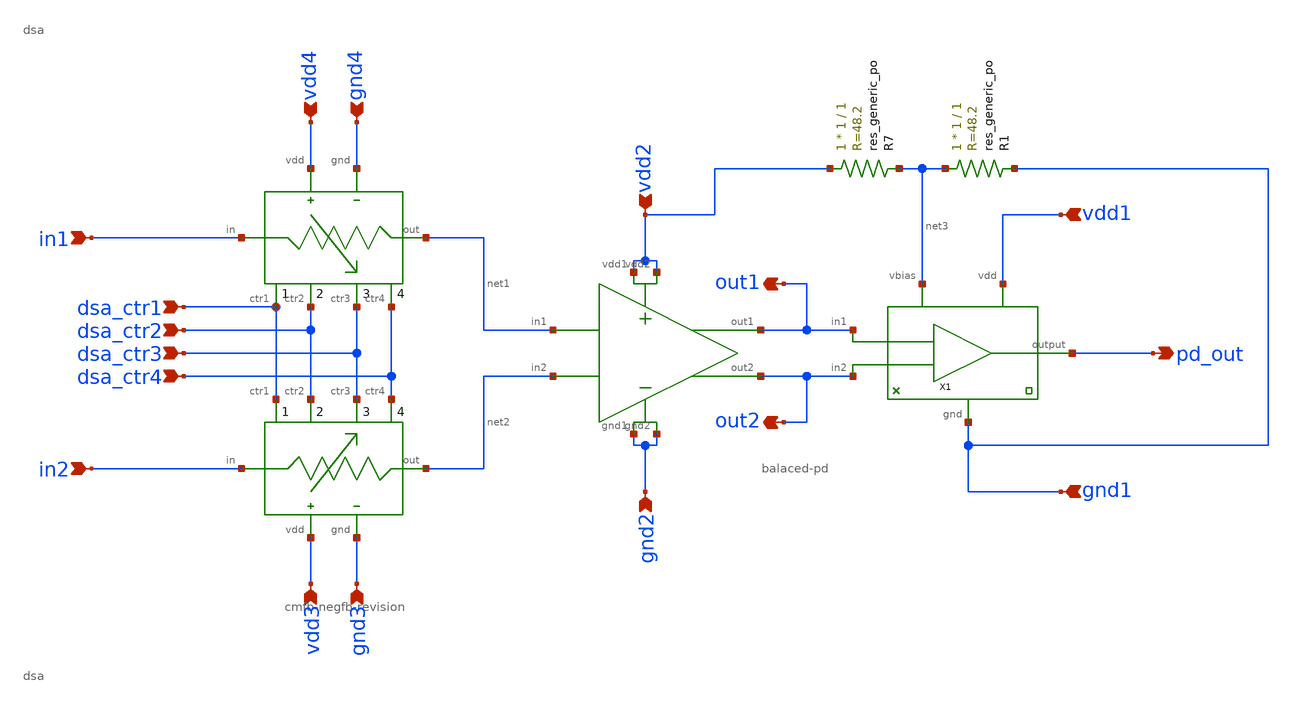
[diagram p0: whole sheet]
** sch_path: xschem/user_analog_project_wrapper.sch
**.subckt user_analog_project_wrapper in1 in2 vdd1 gnd1 dsa_ctr1 dsa_ctr2 dsa_ctr3 dsa_ctr4 pd_out
*+ out1 out2 gnd2 gnd3 gnd4 vdd2 vdd3 vdd4
*.ipin in1
*.ipin in2
*.ipin vdd1
*.ipin gnd1
*.ipin dsa_ctr1
*.ipin dsa_ctr2
*.ipin dsa_ctr3
*.ipin dsa_ctr4
*.opin pd_out
*.opin out1
*.opin out2
*.ipin gnd2
*.ipin gnd3
*.ipin gnd4
*.ipin vdd2
*.ipin vdd3
*.ipin vdd4
XDSA1 dsa_ctr1 dsa_ctr2 dsa_ctr3 dsa_ctr4 in2 vdd3 gnd3 net2 dsa
XDSA2 dsa_ctr1 dsa_ctr2 dsa_ctr3 dsa_ctr4 in1 vdd4 gnd4 net1 dsa
XLNA1 vdd2 vdd2 net1 net2 out1 out2 gnd2 gnd2 cmfb-negfb-revision
X1 out1 out2 net3 vdd1 pd_out gnd1 balaced-pd
XR7 vdd2 net3 sky130_fd_pr__res_generic_po W=1 L=1 m=1
XR1 net3 gnd1 sky130_fd_pr__res_generic_po W=1 L=1 m=1
**** begin user architecture code
 ** manual skywater pdks install (with patches applied)
* .lib $::SKYWATER_MODELS/models/sky130.lib.spice tt

** opencircuitdesign pdks install
.lib $::SKYWATER_MODELS/sky130.lib.spice tt

.param mc_mm_switch=0
.param mc_pr_switch=0

**** end user architecture code
**.ends

* expanding   symbol:  /Volumes/WORK_DRIVE/caravel_automatic_gain_control/xschem/attenuator/dsa.sym
*+ # of pins=8
** sym_path: xschem/attenuator/dsa.sym
** sch_path: xschem/attenuator/dsa.sch
.subckt dsa ctr1 ctr2 ctr3 ctr4 in vdd gnd out
*.ipin in
*.ipin gnd
*.ipin vdd
*.ipin ctr1
*.ipin ctr2
*.ipin ctr3
*.ipin ctr4
*.opin out
XSPDT1 in ctr1 net1 net2 gnd vdd spdt
XSPDT2 net2 ctr2 net3 net4 gnd vdd spdt
XSPDT3 net4 ctr3 net5 net6 gnd vdd spdt
XSPDT4 net6 ctr4 net7 out gnd vdd spdt
XR1 net1 net2 gnd sky130_fd_pr__res_xhigh_po_0p35 L=1 mult=1 m=1
XR2 net4 net3 gnd sky130_fd_pr__res_xhigh_po_0p35 L=1 mult=1 m=1
XR3 net5 net6 gnd sky130_fd_pr__res_xhigh_po_0p35 L=1 mult=1 m=1
XR4 net7 out gnd sky130_fd_pr__res_xhigh_po_0p35 L=1 mult=1 m=1
.ends


* expanding   symbol:
*+  /Volumes/WORK_DRIVE/caravel_automatic_gain_control/xschem/lownoiseamplifier/cmfb-negfb-revision.sym # of pins=8
** sym_path: xschem/lownoiseamplifier/cmfb-negfb-revision.sym
** sch_path: xschem/lownoiseamplifier/cmfb-negfb-revision.sch
.subckt cmfb-negfb-revision vdd1 vdd2 in1 in2 out1 out2 gnd1 gnd2
*.ipin gnd1
*.ipin gnd2
*.ipin vdd1
*.ipin vdd2
*.ipin in1
*.ipin in2
*.opin out1
*.opin out2
XM1 out1 net4 net1 gnd1 sky130_fd_pr__nfet_01v8 L=0.15 W=5 nf=1 ad='int((nf+1)/2) * W/nf * 0.29' as='int((nf+2)/2) * W/nf * 0.29'
+ pd='2*int((nf+1)/2) * (W/nf + 0.29)' ps='2*int((nf+2)/2) * (W/nf + 0.29)' nrd='0.29 / W' nrs='0.29 / W'
+ sa=0 sb=0 sd=0 mult=1 m=1
XM2 out2 net5 net1 gnd1 sky130_fd_pr__nfet_01v8 L=0.15 W=5 nf=1 ad='int((nf+1)/2) * W/nf * 0.29' as='int((nf+2)/2) * W/nf * 0.29'
+ pd='2*int((nf+1)/2) * (W/nf + 0.29)' ps='2*int((nf+2)/2) * (W/nf + 0.29)' nrd='0.29 / W' nrs='0.29 / W'
+ sa=0 sb=0 sd=0 mult=1 m=1
XM3 net2 net2 gnd2 gnd2 sky130_fd_pr__nfet_01v8 L=0.15 W=40 nf=1 ad='int((nf+1)/2) * W/nf * 0.29' as='int((nf+2)/2) * W/nf * 0.29'
+ pd='2*int((nf+1)/2) * (W/nf + 0.29)' ps='2*int((nf+2)/2) * (W/nf + 0.29)' nrd='0.29 / W' nrs='0.29 / W'
+ sa=0 sb=0 sd=0 mult=1 m=1
XM4 net1 net2 gnd2 gnd2 sky130_fd_pr__nfet_01v8 L=0.15 W=40 nf=1 ad='int((nf+1)/2) * W/nf * 0.29' as='int((nf+2)/2) * W/nf * 0.29'
+ pd='2*int((nf+1)/2) * (W/nf + 0.29)' ps='2*int((nf+2)/2) * (W/nf + 0.29)' nrd='0.29 / W' nrs='0.29 / W'
+ sa=0 sb=0 sd=0 mult=1 m=1
XM5 out1 net3 vdd2 vdd2 sky130_fd_pr__pfet_01v8 L=0.15 W=16 nf=1 ad='int((nf+1)/2) * W/nf * 0.29' as='int((nf+2)/2) * W/nf * 0.29'
+ pd='2*int((nf+1)/2) * (W/nf + 0.29)' ps='2*int((nf+2)/2) * (W/nf + 0.29)' nrd='0.29 / W' nrs='0.29 / W'
+ sa=0 sb=0 sd=0 mult=1 m=1
XM6 out2 net3 vdd2 vdd2 sky130_fd_pr__pfet_01v8 L=0.15 W=16 nf=1 ad='int((nf+1)/2) * W/nf * 0.29' as='int((nf+2)/2) * W/nf * 0.29'
+ pd='2*int((nf+1)/2) * (W/nf + 0.29)' ps='2*int((nf+2)/2) * (W/nf + 0.29)' nrd='0.29 / W' nrs='0.29 / W'
+ sa=0 sb=0 sd=0 mult=1 m=1
XR1 out1 net3 sky130_fd_pr__res_generic_po W=1 L=1 m=1
XR2 net3 out2 sky130_fd_pr__res_generic_po W=1 L=1 m=1
XR3 net4 out1 sky130_fd_pr__res_generic_po W=1 L=1 m=1
XR4 out2 net5 sky130_fd_pr__res_generic_po W=1 L=1 m=1
XR5 in1 net4 sky130_fd_pr__res_generic_po W=1 L=1 m=1
XR6 in2 net5 sky130_fd_pr__res_generic_po W=1 L=1 m=1
XR7 vdd1 net2 sky130_fd_pr__res_generic_po W=1 L=1 m=1
.ends


* expanding   symbol:
*+  /Volumes/WORK_DRIVE/caravel_automatic_gain_control/xschem/powerdetector/balaced-pd.sym # of pins=6
** sym_path: xschem/powerdetector/balaced-pd.sym
** sch_path: xschem/powerdetector/balaced-pd.sch
.subckt balaced-pd in1 in2 vbias vdd output gnd
*.ipin vdd
*.ipin gnd
*.opin output
*.ipin in1
*.ipin in2
*.ipin vbias
XM11 output net3 vdd vdd sky130_fd_pr__pfet_01v8 L=0.15 W=1 nf=1 ad='int((nf+1)/2) * W/nf * 0.29' as='int((nf+2)/2) * W/nf * 0.29'
+ pd='2*int((nf+1)/2) * (W/nf + 0.29)' ps='2*int((nf+2)/2) * (W/nf + 0.29)' nrd='0.29 / W' nrs='0.29 / W'
+ sa=0 sb=0 sd=0 mult=1 m=1
XM2 net3 net2 gnd gnd sky130_fd_pr__nfet_01v8 L=0.15 W=2 nf=1 ad='int((nf+1)/2) * W/nf * 0.29' as='int((nf+2)/2) * W/nf * 0.29'
+ pd='2*int((nf+1)/2) * (W/nf + 0.29)' ps='2*int((nf+2)/2) * (W/nf + 0.29)' nrd='0.29 / W' nrs='0.29 / W'
+ sa=0 sb=0 sd=0 mult=1 m=1
XM1 net2 net2 gnd gnd sky130_fd_pr__nfet_01v8 L=0.15 W=2 nf=1 ad='int((nf+1)/2) * W/nf * 0.29' as='int((nf+2)/2) * W/nf * 0.29'
+ pd='2*int((nf+1)/2) * (W/nf + 0.29)' ps='2*int((nf+2)/2) * (W/nf + 0.29)' nrd='0.29 / W' nrs='0.29 / W'
+ sa=0 sb=0 sd=0 mult=1 m=1
XM5 net2 vbias gnd gnd sky130_fd_pr__nfet_01v8 L=0.15 W=2 nf=1 ad='int((nf+1)/2) * W/nf * 0.29' as='int((nf+2)/2) * W/nf * 0.29'
+ pd='2*int((nf+1)/2) * (W/nf + 0.29)' ps='2*int((nf+2)/2) * (W/nf + 0.29)' nrd='0.29 / W' nrs='0.29 / W'
+ sa=0 sb=0 sd=0 mult=1 m=1
XM6 net1 in1 gnd gnd sky130_fd_pr__nfet_01v8 L=0.15 W=2 nf=1 ad='int((nf+1)/2) * W/nf * 0.29' as='int((nf+2)/2) * W/nf * 0.29'
+ pd='2*int((nf+1)/2) * (W/nf + 0.29)' ps='2*int((nf+2)/2) * (W/nf + 0.29)' nrd='0.29 / W' nrs='0.29 / W'
+ sa=0 sb=0 sd=0 mult=1 m=1
XM7 net1 in2 gnd gnd sky130_fd_pr__nfet_01v8 L=0.15 W=2 nf=1 ad='int((nf+1)/2) * W/nf * 0.29' as='int((nf+2)/2) * W/nf * 0.29'
+ pd='2*int((nf+1)/2) * (W/nf + 0.29)' ps='2*int((nf+2)/2) * (W/nf + 0.29)' nrd='0.29 / W' nrs='0.29 / W'
+ sa=0 sb=0 sd=0 mult=1 m=1
XM3 net2 net1 vdd vdd sky130_fd_pr__pfet_01v8 L=0.15 W=1 nf=1 ad='int((nf+1)/2) * W/nf * 0.29' as='int((nf+2)/2) * W/nf * 0.29'
+ pd='2*int((nf+1)/2) * (W/nf + 0.29)' ps='2*int((nf+2)/2) * (W/nf + 0.29)' nrd='0.29 / W' nrs='0.29 / W'
+ sa=0 sb=0 sd=0 mult=1 m=1
XM4 net3 net3 vdd vdd sky130_fd_pr__pfet_01v8 L=0.15 W=1 nf=1 ad='int((nf+1)/2) * W/nf * 0.29' as='int((nf+2)/2) * W/nf * 0.29'
+ pd='2*int((nf+1)/2) * (W/nf + 0.29)' ps='2*int((nf+2)/2) * (W/nf + 0.29)' nrd='0.29 / W' nrs='0.29 / W'
+ sa=0 sb=0 sd=0 mult=1 m=1
XM8 net1 net1 vdd vdd sky130_fd_pr__pfet_01v8 L=0.15 W=1 nf=1 ad='int((nf+1)/2) * W/nf * 0.29' as='int((nf+2)/2) * W/nf * 0.29'
+ pd='2*int((nf+1)/2) * (W/nf + 0.29)' ps='2*int((nf+2)/2) * (W/nf + 0.29)' nrd='0.29 / W' nrs='0.29 / W'
+ sa=0 sb=0 sd=0 mult=1 m=1
.ends


* expanding   symbol:  /Volumes/WORK_DRIVE/caravel_automatic_gain_control/xschem/attenuator/spdt.sym
*+ # of pins=6
** sym_path: xschem/attenuator/spdt.sym
** sch_path: xschem/attenuator/spdt.sch
.subckt spdt in ctr out1 out2 gnd vdd
*.ipin in
*.ipin ctr
*.ipin gnd
*.ipin vdd
*.opin out1
*.opin out2
XINV1 vdd ctr gnd net1 inverter
XTG1 vdd ctr in gnd net1 out1 transgate
XTG2 vdd net1 in gnd ctr out2 transgate
XINV1 vdd ctr gnd net1 inverter
.ends


* expanding   symbol:
*+  /Volumes/WORK_DRIVE/caravel_automatic_gain_control/xschem/attenuator/inverter.sym # of pins=4
** sym_path: xschem/attenuator/inverter.sym
** sch_path: xschem/attenuator/inverter.sch
.subckt inverter vdd in gnd out
*.ipin in
*.ipin gnd
*.ipin vdd
*.opin out
XM1 out in gnd gnd sky130_fd_pr__nfet_01v8 L=0.15 W=4 nf=1 ad='int((nf+1)/2) * W/nf * 0.29' as='int((nf+2)/2) * W/nf * 0.29'
+ pd='2*int((nf+1)/2) * (W/nf + 0.29)' ps='2*int((nf+2)/2) * (W/nf + 0.29)' nrd='0.29 / W' nrs='0.29 / W'
+ sa=0 sb=0 sd=0 mult=1 m=1
XM2 out in vdd vdd sky130_fd_pr__pfet_01v8 L=0.15 W=4 nf=1 ad='int((nf+1)/2) * W/nf * 0.29' as='int((nf+2)/2) * W/nf * 0.29'
+ pd='2*int((nf+1)/2) * (W/nf + 0.29)' ps='2*int((nf+2)/2) * (W/nf + 0.29)' nrd='0.29 / W' nrs='0.29 / W'
+ sa=0 sb=0 sd=0 mult=1 m=1
.ends


* expanding   symbol:
*+  /Volumes/WORK_DRIVE/caravel_automatic_gain_control/xschem/attenuator/transgate.sym # of pins=6
** sym_path: xschem/attenuator/transgate.sym
** sch_path: xschem/attenuator/transgate.sch
.subckt transgate vdd ctr2 in gnd ctr1 out
*.ipin in
*.ipin ctr2
*.ipin ctr1
*.ipin vdd
*.ipin gnd
*.opin out
XM1 in ctr1 out gnd sky130_fd_pr__nfet_01v8 L=0.15 W=4 nf=1 ad='int((nf+1)/2) * W/nf * 0.29' as='int((nf+2)/2) * W/nf * 0.29'
+ pd='2*int((nf+1)/2) * (W/nf + 0.29)' ps='2*int((nf+2)/2) * (W/nf + 0.29)' nrd='0.29 / W' nrs='0.29 / W'
+ sa=0 sb=0 sd=0 mult=1 m=1
XM2 in ctr2 out vdd sky130_fd_pr__pfet_01v8 L=0.15 W=4 nf=1 ad='int((nf+1)/2) * W/nf * 0.29' as='int((nf+2)/2) * W/nf * 0.29'
+ pd='2*int((nf+1)/2) * (W/nf + 0.29)' ps='2*int((nf+2)/2) * (W/nf + 0.29)' nrd='0.29 / W' nrs='0.29 / W'
+ sa=0 sb=0 sd=0 mult=1 m=1
.ends

.end
